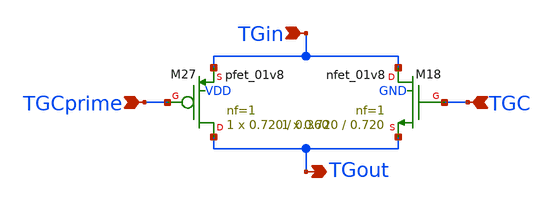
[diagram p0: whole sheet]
** sch_path: xschem/Transmission_Gate.sch
**.subckt Transmission_Gate TGin TGCprime TGout TGC
*.ipin TGin
*.ipin TGCprime
*.opin TGout
*.ipin TGC
XM27 TGout TGCprime TGin VDD sky130_fd_pr__pfet_01v8 L=0.360 W=0.720 nf=1 ad='int((1 + 1)/2) * 0.720 / 1 * 0.29'
+ as='int((1 + 2)/2) * 0.720 / 1 * 0.29' pd='2*int((1 + 1)/2) * (0.720 / 1 + 0.29)' ps='2*int((1 + 2)/2) * (0.720 / 1 + 0.29)'
+ nrd='0.29 / 0.720 ' nrs='0.29 / 0.720 ' sa=0 sb=0 sd=0 mult=1 m=1
XM18 TGin TGC TGout GND sky130_fd_pr__nfet_01v8 L=0.720 W=0.720 nf=1 ad='int((nf+1)/2) * W/nf * 0.29'
+ as='int((nf+2)/2) * W/nf * 0.29' pd='2*int((nf+1)/2) * (W/nf + 0.29)' ps='2*int((nf+2)/2) * (W/nf + 0.29)'
+ nrd='0.29 / W' nrs='0.29 / W' sa=0 sb=0 sd=0 mult=1 m=1
**.ends
.end
